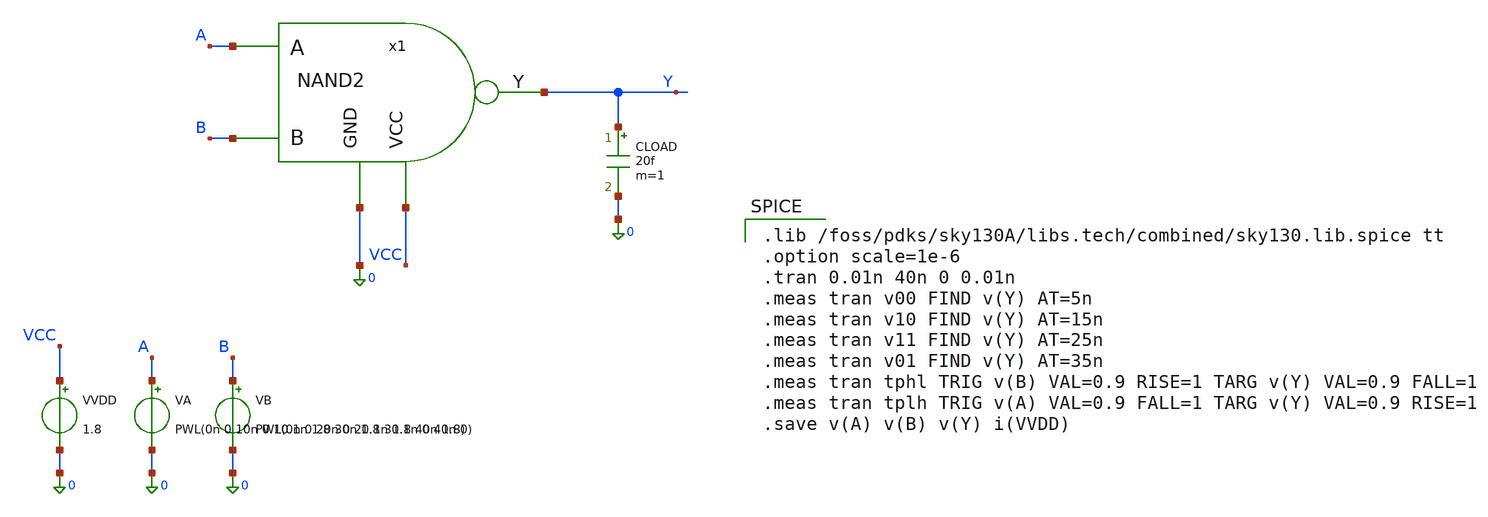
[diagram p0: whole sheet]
** sch_path: blocks/03_StrongARM/sim/tb_NAND2.sch
**.subckt tb_NAND2
VVDD VCC 0 1.8
VA A 0 PWL(0n 0 10n 0 10.1n 1.8 30n 1.8 30.1n 0 40n 0)
VB B 0 PWL(0n 0 20n 0 20.1n 1.8 40n 1.8)
CLOAD Y 0 20f m=1
x1 A B Y 0 VCC NAND2
**** begin user architecture code

.lib /foss/pdks/sky130A/libs.tech/combined/sky130.lib.spice tt
.option scale=1e-6
.tran 0.01n 40n 0 0.01n
.meas tran v00 FIND v(Y) AT=5n
.meas tran v10 FIND v(Y) AT=15n
.meas tran v11 FIND v(Y) AT=25n
.meas tran v01 FIND v(Y) AT=35n
.meas tran tphl TRIG v(B) VAL=0.9 RISE=1 TARG v(Y) VAL=0.9 FALL=1
.meas tran tplh TRIG v(A) VAL=0.9 FALL=1 TARG v(Y) VAL=0.9 RISE=1
.save v(A) v(B) v(Y) i(VVDD)

**** end user architecture code
**.ends

* expanding   symbol:  blocks/03_StrongARM/xschem/NAND2.sym # of pins=5
** sym_path: blocks/03_StrongARM/xschem/NAND2.sym
** sch_path: blocks/03_StrongARM/xschem/NAND2.sch
.subckt NAND2 A B Y GND VCC
*.ipin A
*.ipin B
*.opin Y
*.iopin GND
*.iopin VCC
XMP1 Y A VCC VCC sky130_fd_pr__pfet_01v8 L=0.15 W=2 nf=1 ad='int((1 + 1)/2) * 2 / 1 * 0.29' as='int((1 + 2)/2) * 2 / 1 * 0.29'
+ pd='2*int((1 + 1)/2) * (2 / 1 + 0.29)' ps='2*int((1 + 2)/2) * (2 / 1 + 0.29)' nrd='0.29 / 2 ' nrs='0.29 / 2 '
+ sa=0 sb=0 sd=0 mult=1 m=1
XMP2 Y B VCC VCC sky130_fd_pr__pfet_01v8 L=0.15 W=2 nf=1 ad='int((1 + 1)/2) * 2 / 1 * 0.29' as='int((1 + 2)/2) * 2 / 1 * 0.29'
+ pd='2*int((1 + 1)/2) * (2 / 1 + 0.29)' ps='2*int((1 + 2)/2) * (2 / 1 + 0.29)' nrd='0.29 / 2 ' nrs='0.29 / 2 '
+ sa=0 sb=0 sd=0 mult=1 m=1
XMN1 Y A net1 GND sky130_fd_pr__nfet_01v8 L=0.15 W=2 nf=1 ad='int((1 + 1)/2) * 2 / 1 * 0.29' as='int((1 + 2)/2) * 2 / 1 * 0.29'
+ pd='2*int((1 + 1)/2) * (2 / 1 + 0.29)' ps='2*int((1 + 2)/2) * (2 / 1 + 0.29)' nrd='0.29 / 2 ' nrs='0.29 / 2 '
+ sa=0 sb=0 sd=0 mult=1 m=1
XMN2 net1 B GND GND sky130_fd_pr__nfet_01v8 L=0.15 W=2 nf=1 ad='int((1 + 1)/2) * 2 / 1 * 0.29' as='int((1 + 2)/2) * 2 / 1 * 0.29'
+ pd='2*int((1 + 1)/2) * (2 / 1 + 0.29)' ps='2*int((1 + 2)/2) * (2 / 1 + 0.29)' nrd='0.29 / 2 ' nrs='0.29 / 2 '
+ sa=0 sb=0 sd=0 mult=1 m=1
.ends

.end
